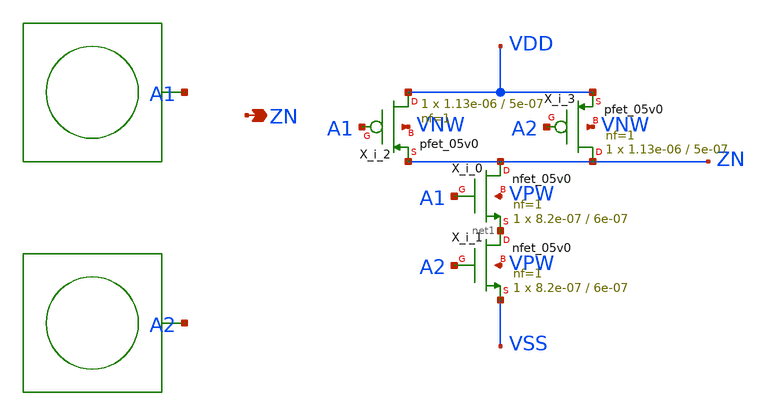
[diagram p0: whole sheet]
** sch_path: project/examples/gf180mcu_nand2/gf180mcu_nand2.sch
**.subckt gf180mcu_nand2 ZN
*.opin ZN
VBUTTON_A1 A1 VSS external
VBUTTON_A2 A2 VSS external
X_i_1 net1 A2 VSS VPW nfet_05v0 L=6e-07 W=8.2e-07 nf=1 ad='int((nf+1)/2) * W/nf * 0.18u' as='int((nf+2)/2) * W/nf * 0.18u'
+ pd='2*int((nf+1)/2) * (W/nf + 0.18u)' ps='2*int((nf+2)/2) * (W/nf + 0.18u)' nrd='0.18u / W' nrs='0.18u / W'
+ sa=0 sb=0 sd=0 m=1
X_i_0 ZN A1 net1 VPW nfet_05v0 L=6e-07 W=8.2e-07 nf=1 ad='int((nf+1)/2) * W/nf * 0.18u' as='int((nf+2)/2) * W/nf * 0.18u'
+ pd='2*int((nf+1)/2) * (W/nf + 0.18u)' ps='2*int((nf+2)/2) * (W/nf + 0.18u)' nrd='0.18u / W' nrs='0.18u / W'
+ sa=0 sb=0 sd=0 m=1
X_i_3 ZN A2 VDD VNW pfet_05v0 L=5e-07 W=1.13e-06 nf=1 ad='int((nf+1)/2) * W/nf * 0.18u' as='int((nf+2)/2) * W/nf * 0.18u'
+ pd='2*int((nf+1)/2) * (W/nf + 0.18u)' ps='2*int((nf+2)/2) * (W/nf + 0.18u)' nrd='0.18u / W' nrs='0.18u / W'
+ sa=0 sb=0 sd=0 m=1
X_i_2 VDD A1 ZN VNW pfet_05v0 L=5e-07 W=1.13e-06 nf=1 ad='int((nf+1)/2) * W/nf * 0.18u' as='int((nf+2)/2) * W/nf * 0.18u'
+ pd='2*int((nf+1)/2) * (W/nf + 0.18u)' ps='2*int((nf+2)/2) * (W/nf + 0.18u)' nrd='0.18u / W' nrs='0.18u / W'
+ sa=0 sb=0 sd=0 m=1
**.ends
.end
